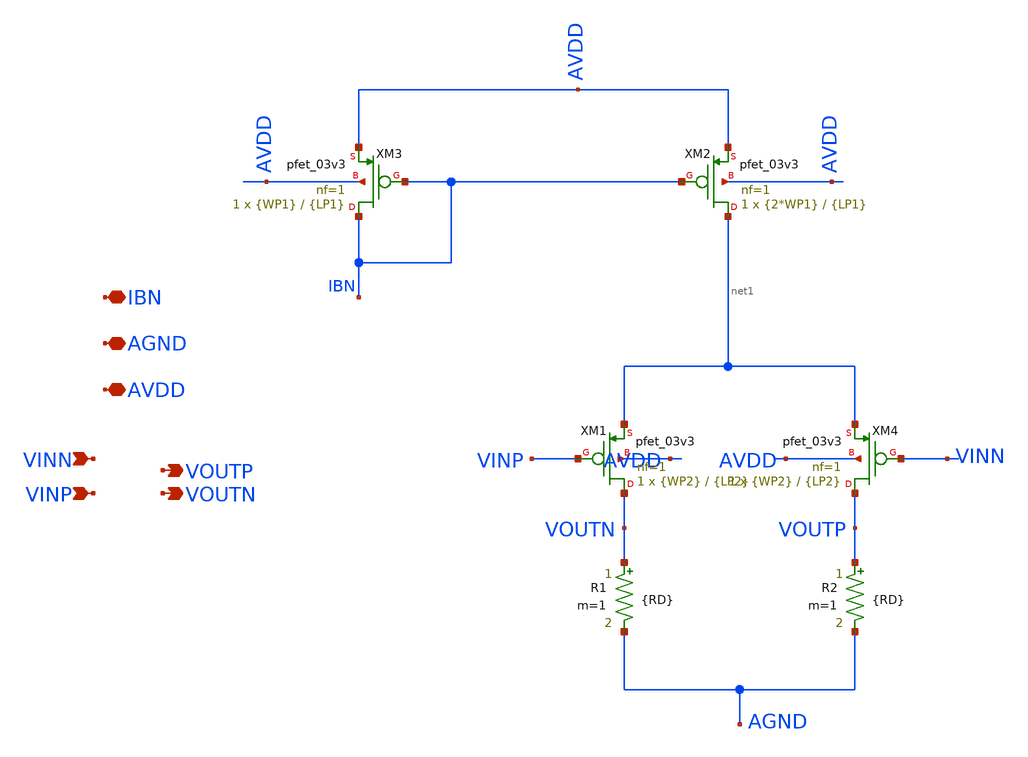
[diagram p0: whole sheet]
** sch_path: Lab_03/DIFFPAIR.sch
**.subckt DIFFPAIR IBN AGND AVDD VINN VINP VOUTP VOUTN
*.iopin IBN
*.iopin AGND
*.iopin AVDD
*.ipin VINN
*.ipin VINP
*.opin VOUTP
*.opin VOUTN
XM3 IBN IBN AVDD AVDD pfet_03v3 L={LP1} W={WP1} nf=1 ad='int((nf+1)/2) * W/nf * 0.18u' as='int((nf+2)/2) * W/nf * 0.18u'
+ pd='2*int((nf+1)/2) * (W/nf + 0.18u)' ps='2*int((nf+2)/2) * (W/nf + 0.18u)' nrd='0.18u / W' nrs='0.18u / W'
+ sa=0 sb=0 sd=0 m=1
XM4 VOUTP VINN net1 AVDD pfet_03v3 L={LP2} W={WP2} nf=1 ad='int((nf+1)/2) * W/nf * 0.18u' as='int((nf+2)/2) * W/nf * 0.18u'
+ pd='2*int((nf+1)/2) * (W/nf + 0.18u)' ps='2*int((nf+2)/2) * (W/nf + 0.18u)' nrd='0.18u / W' nrs='0.18u / W'
+ sa=0 sb=0 sd=0 m=1
R1 VOUTN AGND {RD} m=1
R2 VOUTP AGND {RD} m=1
XM1 VOUTN VINP net1 AVDD pfet_03v3 L={LP2} W={WP2} nf=1 ad='int((nf+1)/2) * W/nf * 0.18u' as='int((nf+2)/2) * W/nf * 0.18u'
+ pd='2*int((nf+1)/2) * (W/nf + 0.18u)' ps='2*int((nf+2)/2) * (W/nf + 0.18u)' nrd='0.18u / W' nrs='0.18u / W'
+ sa=0 sb=0 sd=0 m=1
XM2 net1 IBN AVDD AVDD pfet_03v3 L={LP1} W={2*WP1} nf=1 ad='int((nf+1)/2) * W/nf * 0.18u' as='int((nf+2)/2) * W/nf * 0.18u'
+ pd='2*int((nf+1)/2) * (W/nf + 0.18u)' ps='2*int((nf+2)/2) * (W/nf + 0.18u)' nrd='0.18u / W' nrs='0.18u / W'
+ sa=0 sb=0 sd=0 m=1
**.ends
.end
